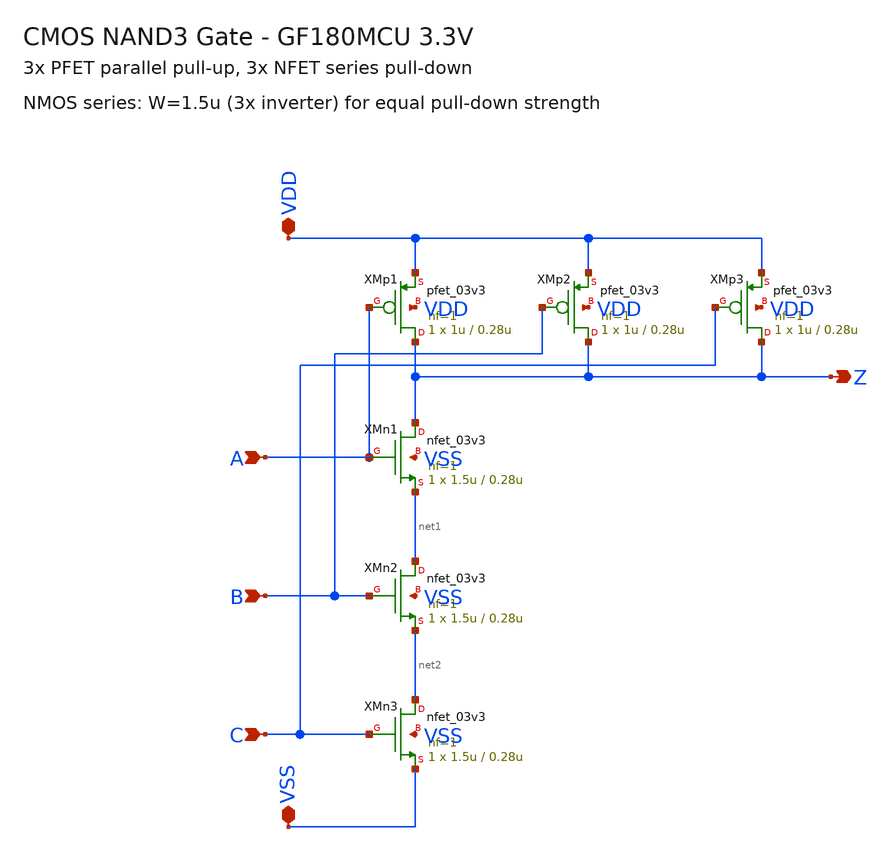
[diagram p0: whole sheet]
** sch_path: designs/libs/core_analog/pfd/nand3_pf.sch
**.subckt nand3_pf VDD VSS A B C Z
*.iopin VDD
*.iopin VSS
*.ipin A
*.ipin B
*.ipin C
*.opin Z
XMp1 Z A VDD VDD pfet_03v3 L=0.28u W=1u nf=1 ad='int((nf+1)/2) * W/nf * 0.18u' as='int((nf+2)/2) * W/nf * 0.18u'
+ pd='2*int((nf+1)/2) * (W/nf + 0.18u)' ps='2*int((nf+2)/2) * (W/nf + 0.18u)' nrd='0.18u / W' nrs='0.18u / W'
+ sa=0 sb=0 sd=0 m=1
XMp2 Z B VDD VDD pfet_03v3 L=0.28u W=1u nf=1 ad='int((nf+1)/2) * W/nf * 0.18u' as='int((nf+2)/2) * W/nf * 0.18u'
+ pd='2*int((nf+1)/2) * (W/nf + 0.18u)' ps='2*int((nf+2)/2) * (W/nf + 0.18u)' nrd='0.18u / W' nrs='0.18u / W'
+ sa=0 sb=0 sd=0 m=1
XMp3 Z C VDD VDD pfet_03v3 L=0.28u W=1u nf=1 ad='int((nf+1)/2) * W/nf * 0.18u' as='int((nf+2)/2) * W/nf * 0.18u'
+ pd='2*int((nf+1)/2) * (W/nf + 0.18u)' ps='2*int((nf+2)/2) * (W/nf + 0.18u)' nrd='0.18u / W' nrs='0.18u / W'
+ sa=0 sb=0 sd=0 m=1
XMn1 Z A net1 VSS nfet_03v3 L=0.28u W=1.5u nf=1 ad='int((nf+1)/2) * W/nf * 0.18u' as='int((nf+2)/2) * W/nf * 0.18u'
+ pd='2*int((nf+1)/2) * (W/nf + 0.18u)' ps='2*int((nf+2)/2) * (W/nf + 0.18u)' nrd='0.18u / W' nrs='0.18u / W'
+ sa=0 sb=0 sd=0 m=1
XMn2 net1 B net2 VSS nfet_03v3 L=0.28u W=1.5u nf=1 ad='int((nf+1)/2) * W/nf * 0.18u' as='int((nf+2)/2) * W/nf * 0.18u'
+ pd='2*int((nf+1)/2) * (W/nf + 0.18u)' ps='2*int((nf+2)/2) * (W/nf + 0.18u)' nrd='0.18u / W' nrs='0.18u / W'
+ sa=0 sb=0 sd=0 m=1
XMn3 net2 C VSS VSS nfet_03v3 L=0.28u W=1.5u nf=1 ad='int((nf+1)/2) * W/nf * 0.18u' as='int((nf+2)/2) * W/nf * 0.18u'
+ pd='2*int((nf+1)/2) * (W/nf + 0.18u)' ps='2*int((nf+2)/2) * (W/nf + 0.18u)' nrd='0.18u / W' nrs='0.18u / W'
+ sa=0 sb=0 sd=0 m=1
**.ends
.end
